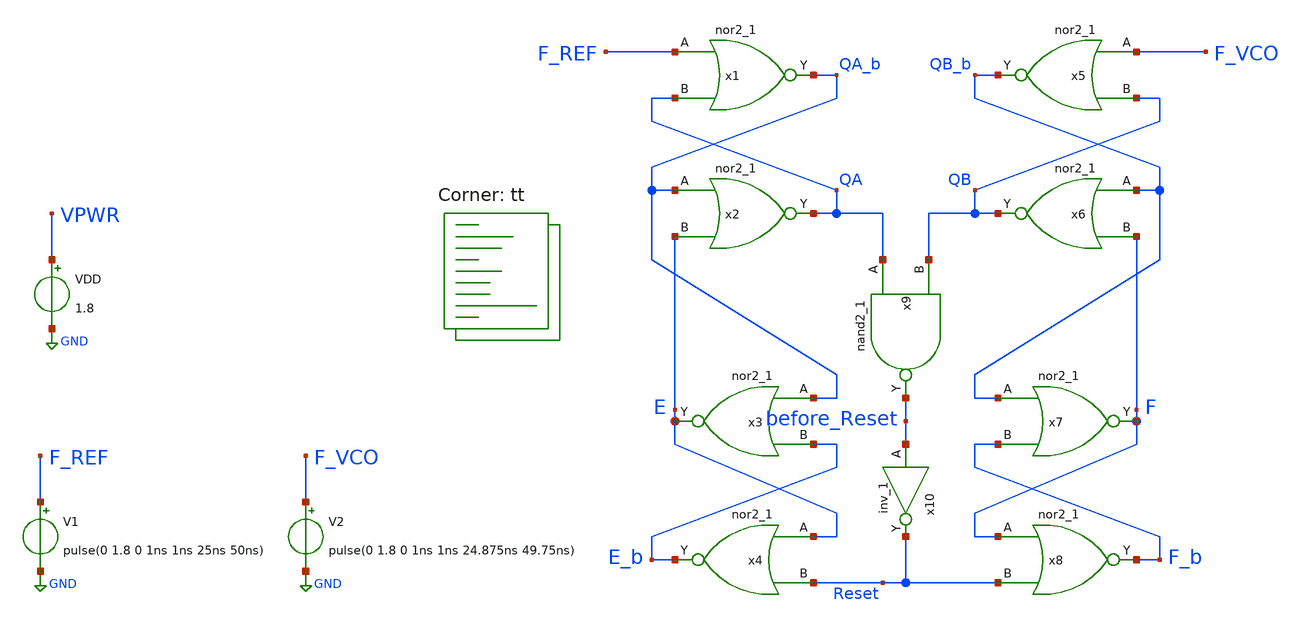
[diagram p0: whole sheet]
** sch_path: projects/pll/pfd/xschem_ngspice/phase_frequency_detector2.sch
**.subckt phase_frequency_detector2
x1 F_REF QA GND GND VPWR VPWR QA_b sky130_fd_sc_hd__nor2_1
x2 QA_b E GND GND VPWR VPWR QA sky130_fd_sc_hd__nor2_1
x3 QA_b E_b GND GND VPWR VPWR E sky130_fd_sc_hd__nor2_1
x4 E Reset GND GND VPWR VPWR E_b sky130_fd_sc_hd__nor2_1
x5 F_VCO QB GND GND VPWR VPWR QB_b sky130_fd_sc_hd__nor2_1
x6 QB_b F GND GND VPWR VPWR QB sky130_fd_sc_hd__nor2_1
x7 QB_b F_b GND GND VPWR VPWR F sky130_fd_sc_hd__nor2_1
x8 F Reset GND GND VPWR VPWR F_b sky130_fd_sc_hd__nor2_1
x9 QA QB GND GND VPWR VPWR before_Reset sky130_fd_sc_hd__nand2_1
x10 before_Reset GND GND VPWR VPWR Reset sky130_fd_sc_hd__inv_1
V1 F_REF GND pulse(0 1.8 0 1ns 1ns 25ns 50ns)
V2 F_VCO GND pulse(0 1.8 0 1ns 1ns 24.875ns 49.75ns)
VDD VPWR GND 1.8
**** begin user architecture code
.lib $::SKYWATER_MODELS/sky130.lib.spice tt



* .lib /foss/pdks/sky130A/libs.tech/ngspice/sky130.lib.spice tt
.include /foss/pdks/sky130A/libs.ref/sky130_fd_sc_hd/spice/sky130_fd_sc_hd.spice


.option wnflag=1
.option method=gear trtol=1

* .ic v(osc)=0

* .temp = 75

.control

    save all
    tran 1ns 10us
    remzerovec
    write phase_frequency_detector.raw
    * wrdata /foss/designs/my_design/projects/pll/pfd/xschem_ngspice/phase_frequency_detector.txt
    set appendwrite

.endc






**** end user architecture code
**.ends
.GLOBAL GND
.end
